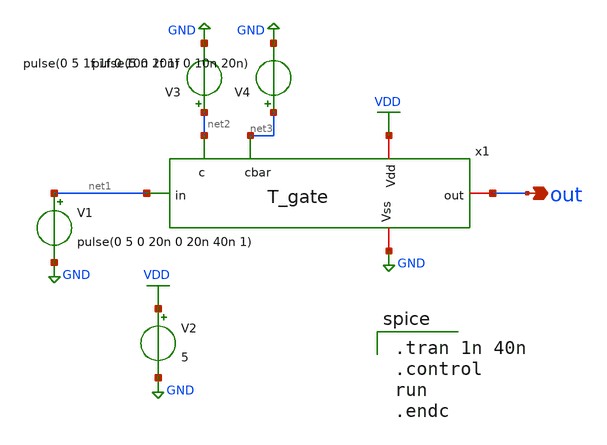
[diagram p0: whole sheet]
** sch_path: ADC/4bit_C2C/MagicAndSpice/T_gate_TB.sch
**.subckt T_gate_TB out
*.opin out
V1 net1 GND pulse(0 5 0 20n 0 20n 40n 1)
V2 VDD GND 5
V3 net2 GND pulse(0 5 1f 1f 0 10n 20n)
V4 net3 GND pulse(5 0 1f 1f 0 10n 20n)
x1 net2 out net1 VDD net3 GND T_gate
**** begin user architecture code

** opencircuitdesign pdks install
.lib $::SKYWATER_MODELS/sky130.lib.spice tt



.tran 1n 40n
.control
run
.endc

**** end user architecture code
**.ends
.GLOBAL GND
.GLOBAL VDD
.end
